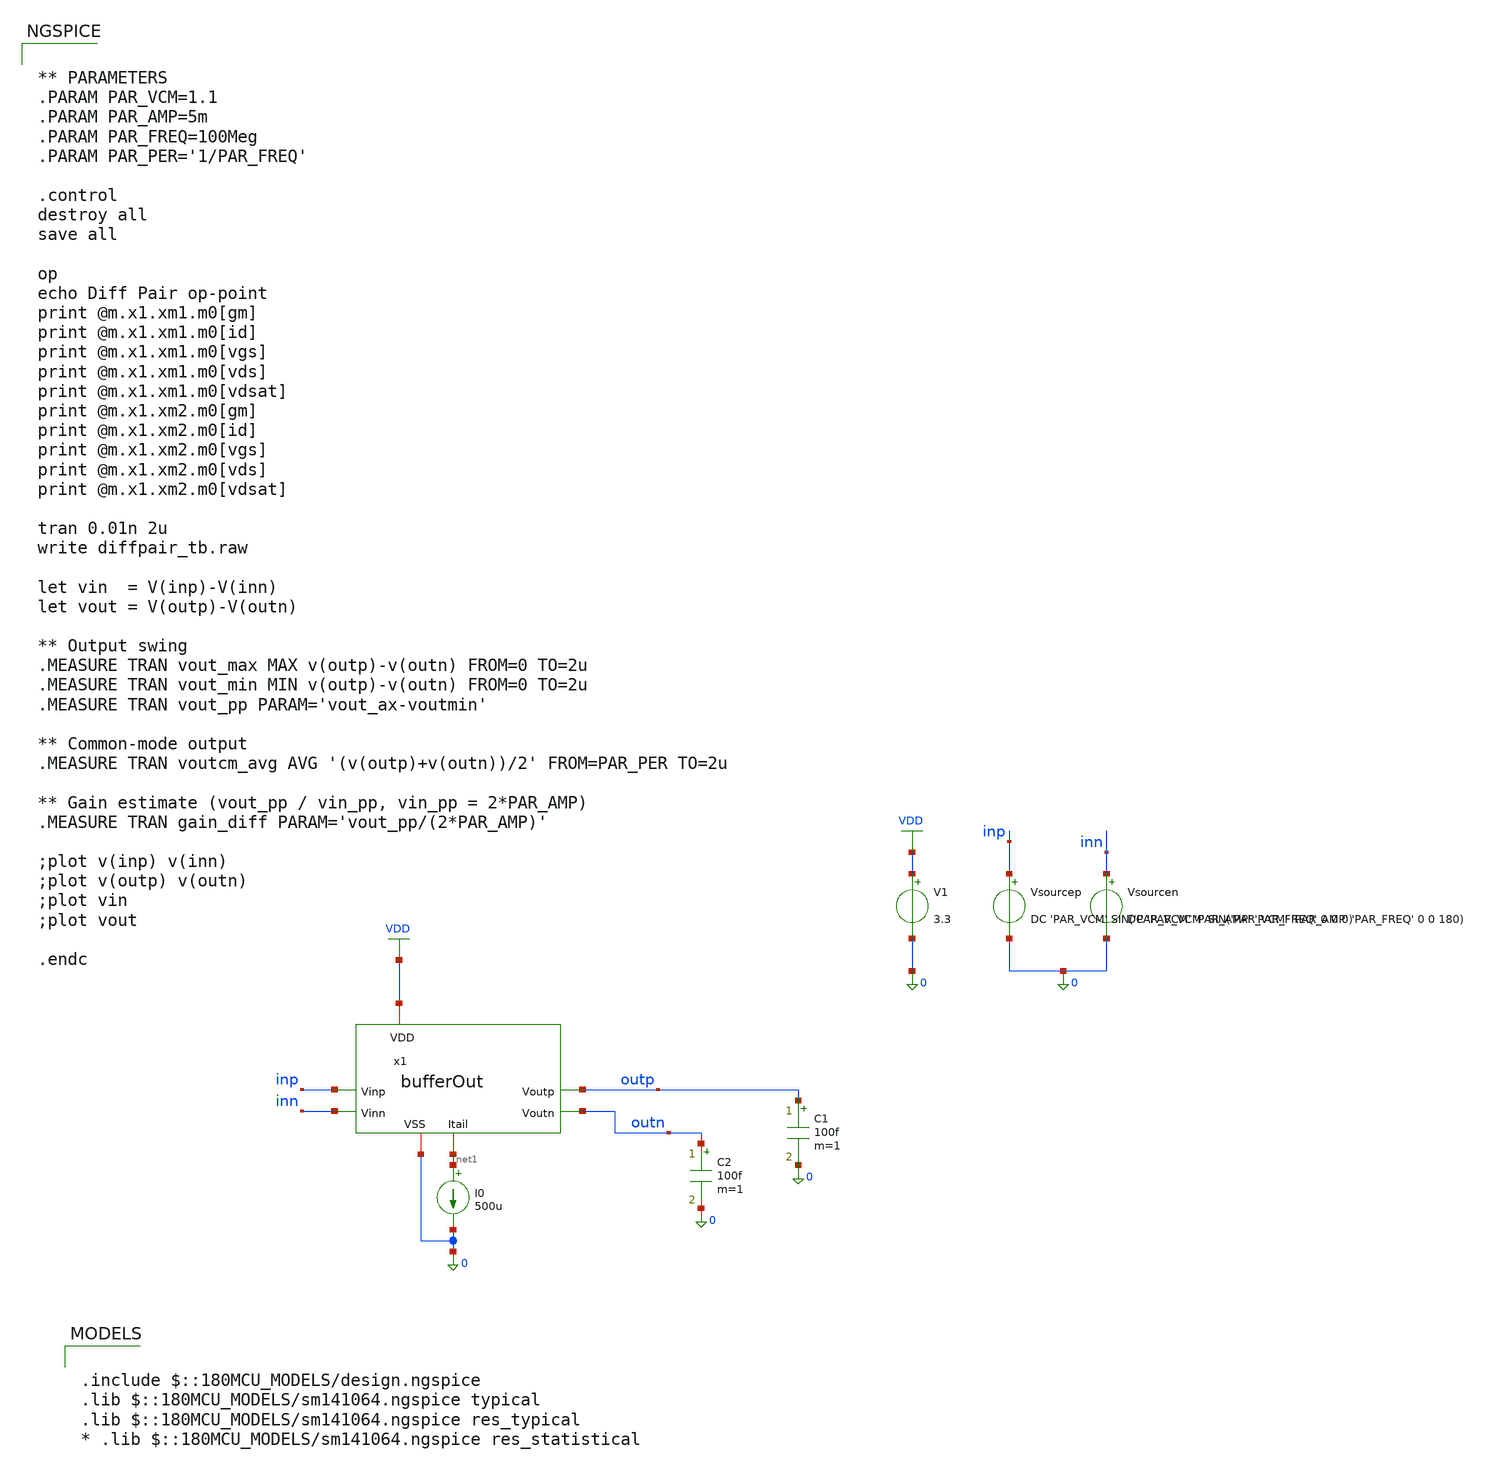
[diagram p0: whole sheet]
** sch_path: designs/output_buffer/testbench/bufferOut_tb.sch
**.subckt bufferOut_tb
V1 VDD 0 3.3
Vsourcep inp 0 DC 'PAR_VCM' SIN('PAR_VCM' 'PAR_AMP' 'PAR_FREQ' 0 0 0)
Vsourcen inn 0 DC 'PAR_VCM' SIN('PAR_VCM' 'PAR_AMP' 'PAR_FREQ' 0 0 180)
I0 net1 0 500u
C1 outp 0 100f m=1
C2 outn 0 100f m=1
x1 VDD 0 net1 outp outn inp inn bufferOut
**** begin user architecture code

.include $::180MCU_MODELS/design.ngspice
.lib $::180MCU_MODELS/sm141064.ngspice typical
.lib $::180MCU_MODELS/sm141064.ngspice res_typical
* .lib $::180MCU_MODELS/sm141064.ngspice res_statistical



** PARAMETERS
.PARAM PAR_VCM=1.1
.PARAM PAR_AMP=5m
.PARAM PAR_FREQ=100Meg
.PARAM PAR_PER='1/PAR_FREQ'

.control
destroy all
save all

op
echo Diff Pair op-point
print @m.x1.xm1.m0[gm]
print @m.x1.xm1.m0[id]
print @m.x1.xm1.m0[vgs]
print @m.x1.xm1.m0[vds]
print @m.x1.xm1.m0[vdsat]
print @m.x1.xm2.m0[gm]
print @m.x1.xm2.m0[id]
print @m.x1.xm2.m0[vgs]
print @m.x1.xm2.m0[vds]
print @m.x1.xm2.m0[vdsat]

tran 0.01n 2u
write diffpair_tb.raw

let vin  = V(inp)-V(inn)
let vout = V(outp)-V(outn)

** Output swing
.MEASURE TRAN vout_max MAX v(outp)-v(outn) FROM=0 TO=2u
.MEASURE TRAN vout_min MIN v(outp)-v(outn) FROM=0 TO=2u
.MEASURE TRAN vout_pp PARAM='vout_ax-voutmin'

** Common-mode output
.MEASURE TRAN voutcm_avg AVG '(v(outp)+v(outn))/2' FROM=PAR_PER TO=2u

** Gain estimate (vout_pp / vin_pp, vin_pp = 2*PAR_AMP)
.MEASURE TRAN gain_diff PARAM='vout_pp/(2*PAR_AMP)'

;plot v(inp) v(inn)
;plot v(outp) v(outn)
;plot vin
;plot vout

.endc


**** end user architecture code
**.ends

* expanding   symbol:  bufferOut.sym # of pins=7
** sym_path: designs/output_buffer/schematic/bufferOut.sym
** sch_path: designs/output_buffer/schematic/bufferOut.sch
.subckt bufferOut VDD VSS Itail Voutp Voutn Vinp Vinn
*.iopin VDD
*.iopin Itail
*.iopin VSS
*.ipin Vinp
*.ipin Vinn
*.opin Voutp
*.opin Voutn
XM1 Voutp Vinp Itail VSS nfet_03v3 L=0.28u W=21u nf=7 ad='int((nf+1)/2) * W/nf * 0.18u' as='int((nf+2)/2) * W/nf * 0.18u'
+ pd='2*int((nf+1)/2) * (W/nf + 0.18u)' ps='2*int((nf+2)/2) * (W/nf + 0.18u)' nrd='0.18u / W' nrs='0.18u / W'
+ sa=0 sb=0 sd=0 m=1
XM2 Voutn Vinn Itail VSS nfet_03v3 L=0.28u W=21u nf=7 ad='int((nf+1)/2) * W/nf * 0.18u' as='int((nf+2)/2) * W/nf * 0.18u'
+ pd='2*int((nf+1)/2) * (W/nf + 0.18u)' ps='2*int((nf+2)/2) * (W/nf + 0.18u)' nrd='0.18u / W' nrs='0.18u / W'
+ sa=0 sb=0 sd=0 m=1
XR1 Voutp VDD VSS ppolyf_u_1k r_width=1e-6 r_length=1.8e-6 m=1
XR2 Voutn VDD VSS ppolyf_u_1k r_width=1e-6 r_length=1.8e-6 m=1
.ends

.GLOBAL VDD
.end
